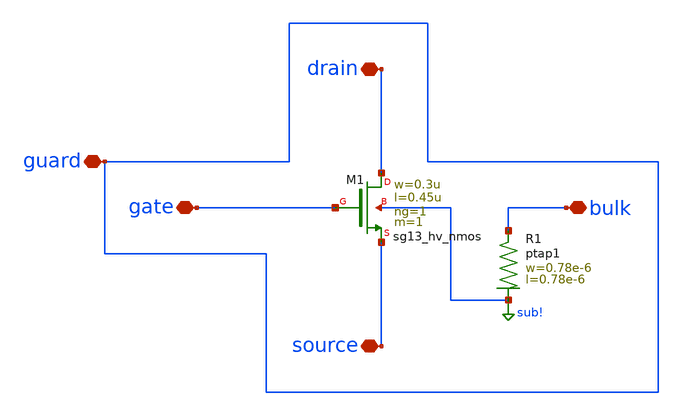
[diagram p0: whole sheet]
** sch_path: trident_test_structures/design_data/xschem/transistor_characterization/hv_nmos_w0u3_l0u45_guarded/hv_nmos_w0u3_l0u45_guarded.sch
**.subckt hv_nmos_w0u3_l0u45_guarded gate drain source bulk guard
*.iopin gate
*.iopin drain
*.iopin source
*.iopin bulk
*.iopin guard
XM1 drain gate source sub! sg13_hv_nmos w=0.3u l=0.45u ng=1 m=1 mm_ok=1
XR1 bulk sub! ptap1 R=262.8 w=0.78e-6 l=0.78e-6
**.ends
.GLOBAL sub!
.end
